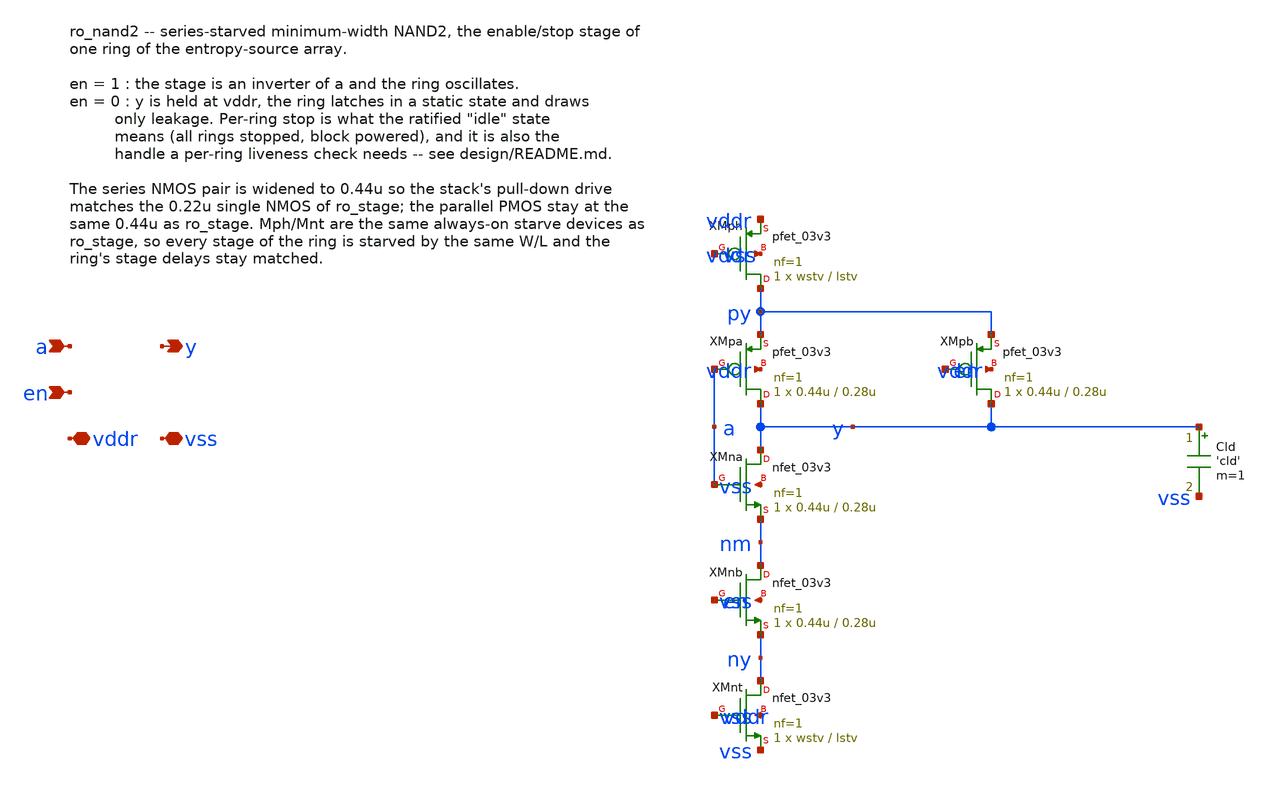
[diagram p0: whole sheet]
** sch_path: design/xschem/ro_nand2.sch
**.subckt ro_nand2 a en y vddr vss
*.ipin a
*.ipin en
*.opin y
*.iopin vddr
*.iopin vss
XMph py vss vddr vddr pfet_03v3 L=lstv W=wstv nf=1 ad='int((nf+1)/2) * W/nf * 0.18u' as='int((nf+2)/2) * W/nf * 0.18u'
+ pd='2*int((nf+1)/2) * (W/nf + 0.18u)' ps='2*int((nf+2)/2) * (W/nf + 0.18u)' nrd='0.18u / W' nrs='0.18u / W'
+ sa=0 sb=0 sd=0 m=1
XMpa y a py vddr pfet_03v3 L=0.28u W=0.44u nf=1 ad='int((nf+1)/2) * W/nf * 0.18u' as='int((nf+2)/2) * W/nf * 0.18u'
+ pd='2*int((nf+1)/2) * (W/nf + 0.18u)' ps='2*int((nf+2)/2) * (W/nf + 0.18u)' nrd='0.18u / W' nrs='0.18u / W'
+ sa=0 sb=0 sd=0 m=1
XMpb y en py vddr pfet_03v3 L=0.28u W=0.44u nf=1 ad='int((nf+1)/2) * W/nf * 0.18u' as='int((nf+2)/2) * W/nf * 0.18u'
+ pd='2*int((nf+1)/2) * (W/nf + 0.18u)' ps='2*int((nf+2)/2) * (W/nf + 0.18u)' nrd='0.18u / W' nrs='0.18u / W'
+ sa=0 sb=0 sd=0 m=1
XMna y a nm vss nfet_03v3 L=0.28u W=0.44u nf=1 ad='int((nf+1)/2) * W/nf * 0.18u' as='int((nf+2)/2) * W/nf * 0.18u'
+ pd='2*int((nf+1)/2) * (W/nf + 0.18u)' ps='2*int((nf+2)/2) * (W/nf + 0.18u)' nrd='0.18u / W' nrs='0.18u / W'
+ sa=0 sb=0 sd=0 m=1
XMnb nm en ny vss nfet_03v3 L=0.28u W=0.44u nf=1 ad='int((nf+1)/2) * W/nf * 0.18u' as='int((nf+2)/2) * W/nf * 0.18u'
+ pd='2*int((nf+1)/2) * (W/nf + 0.18u)' ps='2*int((nf+2)/2) * (W/nf + 0.18u)' nrd='0.18u / W' nrs='0.18u / W'
+ sa=0 sb=0 sd=0 m=1
XMnt ny vddr vss vss nfet_03v3 L=lstv W=wstv nf=1 ad='int((nf+1)/2) * W/nf * 0.18u' as='int((nf+2)/2) * W/nf * 0.18u'
+ pd='2*int((nf+1)/2) * (W/nf + 0.18u)' ps='2*int((nf+2)/2) * (W/nf + 0.18u)' nrd='0.18u / W' nrs='0.18u / W'
+ sa=0 sb=0 sd=0 m=1
Cld y vss 'cld' m=1
**.ends
.end
